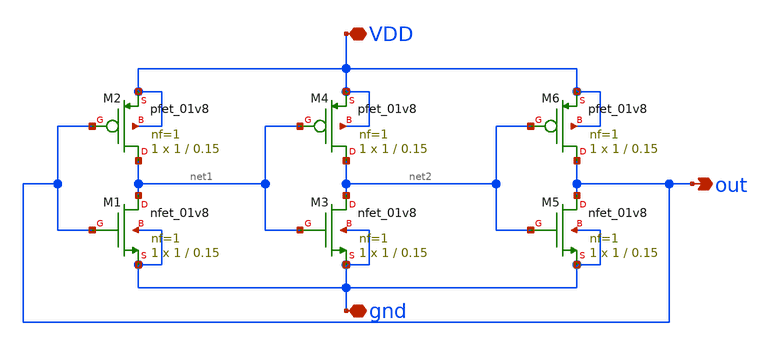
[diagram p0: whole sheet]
** sch_path: week4/ring_osc_pl/untitled.sch
**.subckt untitled gnd VDD out
*.iopin gnd
*.iopin VDD
*.opin out
XM1 net1 out gnd gnd sky130_fd_pr__nfet_01v8 L=0.15 W=1 nf=1 ad='int((nf+1)/2) * W/nf * 0.29' as='int((nf+2)/2) * W/nf * 0.29'
+ pd='2*int((nf+1)/2) * (W/nf + 0.29)' ps='2*int((nf+2)/2) * (W/nf + 0.29)' nrd='0.29 / W' nrs='0.29 / W'
+ sa=0 sb=0 sd=0 mult=1 m=1
XM2 net1 out VDD VDD sky130_fd_pr__pfet_01v8 L=0.15 W=1 nf=1 ad='int((nf+1)/2) * W/nf * 0.29' as='int((nf+2)/2) * W/nf * 0.29'
+ pd='2*int((nf+1)/2) * (W/nf + 0.29)' ps='2*int((nf+2)/2) * (W/nf + 0.29)' nrd='0.29 / W' nrs='0.29 / W'
+ sa=0 sb=0 sd=0 mult=1 m=1
XM3 net2 net1 gnd gnd sky130_fd_pr__nfet_01v8 L=0.15 W=1 nf=1 ad='int((nf+1)/2) * W/nf * 0.29' as='int((nf+2)/2) * W/nf * 0.29'
+ pd='2*int((nf+1)/2) * (W/nf + 0.29)' ps='2*int((nf+2)/2) * (W/nf + 0.29)' nrd='0.29 / W' nrs='0.29 / W'
+ sa=0 sb=0 sd=0 mult=1 m=1
XM4 net2 net1 VDD VDD sky130_fd_pr__pfet_01v8 L=0.15 W=1 nf=1 ad='int((nf+1)/2) * W/nf * 0.29' as='int((nf+2)/2) * W/nf * 0.29'
+ pd='2*int((nf+1)/2) * (W/nf + 0.29)' ps='2*int((nf+2)/2) * (W/nf + 0.29)' nrd='0.29 / W' nrs='0.29 / W'
+ sa=0 sb=0 sd=0 mult=1 m=1
XM5 out net2 gnd gnd sky130_fd_pr__nfet_01v8 L=0.15 W=1 nf=1 ad='int((nf+1)/2) * W/nf * 0.29' as='int((nf+2)/2) * W/nf * 0.29'
+ pd='2*int((nf+1)/2) * (W/nf + 0.29)' ps='2*int((nf+2)/2) * (W/nf + 0.29)' nrd='0.29 / W' nrs='0.29 / W'
+ sa=0 sb=0 sd=0 mult=1 m=1
XM6 out net2 VDD VDD sky130_fd_pr__pfet_01v8 L=0.15 W=1 nf=1 ad='int((nf+1)/2) * W/nf * 0.29' as='int((nf+2)/2) * W/nf * 0.29'
+ pd='2*int((nf+1)/2) * (W/nf + 0.29)' ps='2*int((nf+2)/2) * (W/nf + 0.29)' nrd='0.29 / W' nrs='0.29 / W'
+ sa=0 sb=0 sd=0 mult=1 m=1
**.ends
.end
